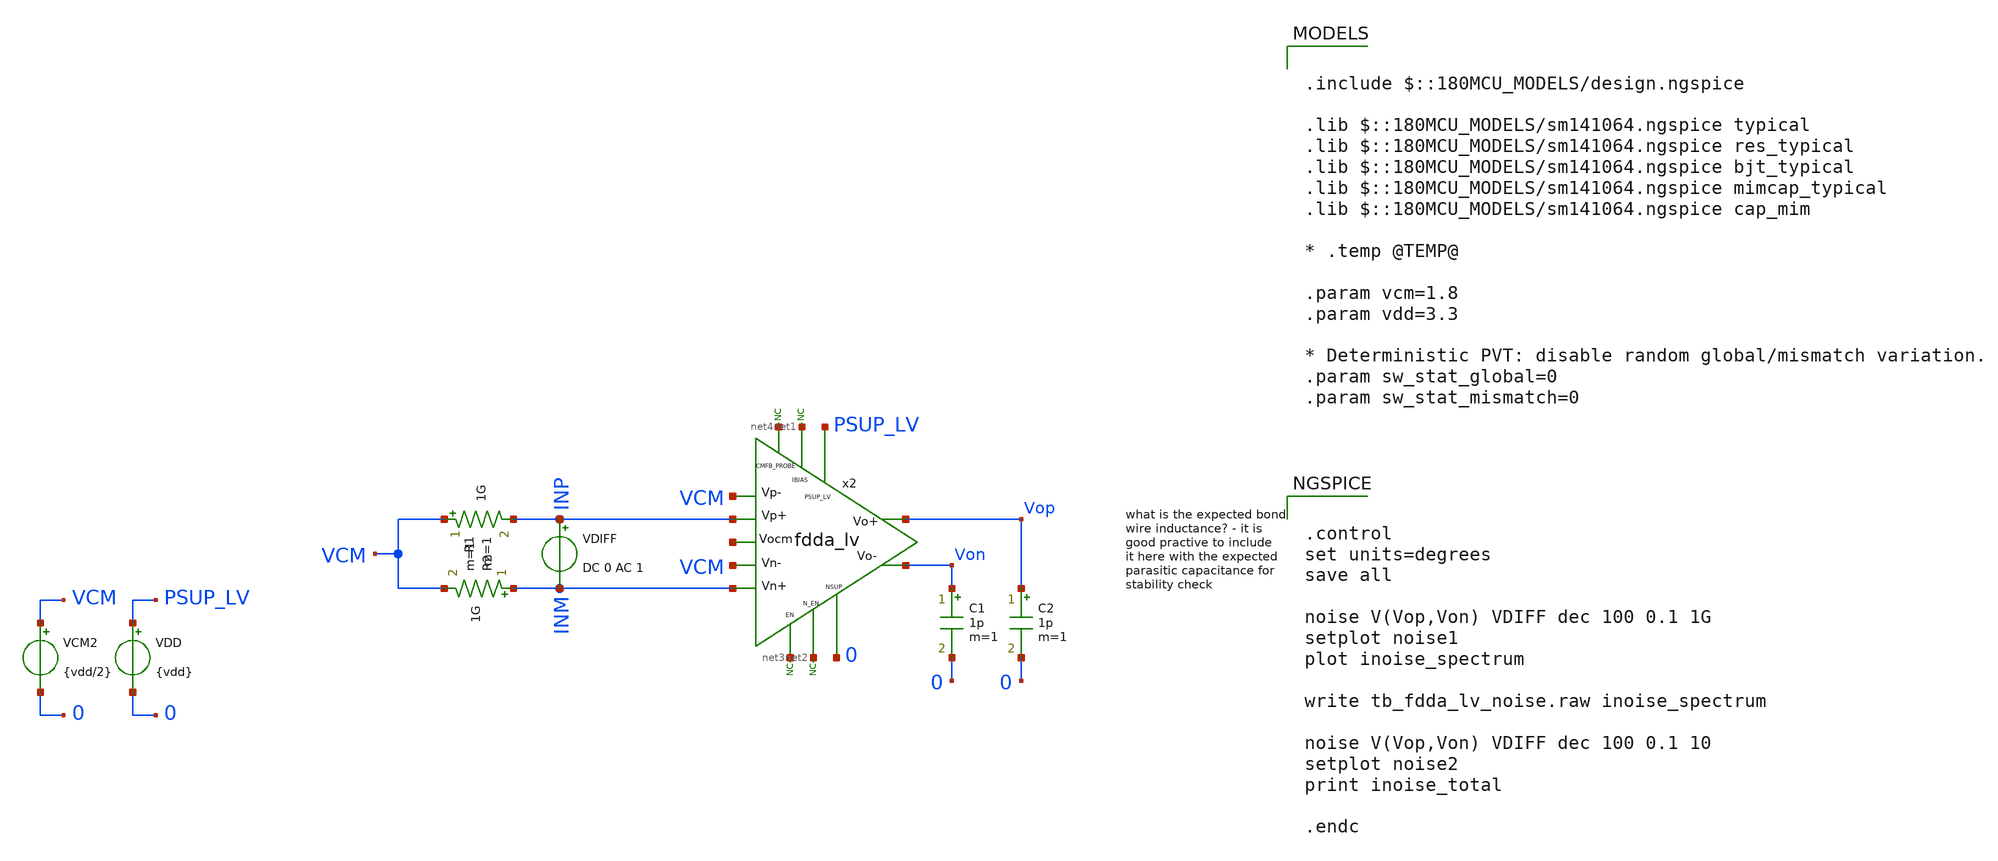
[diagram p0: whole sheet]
** sch_path: xschem/blocks/fdda_lv/tb_fdda_lv_noise.sch
**.subckt tb_fdda_lv_noise
C1 Von 0 1p m=1
x2 PSUP_LV VCM VCM INM INP Vop Von net1 net2 net3 0 net4 net5 fdda_lv
* noconn #net1
* noconn #net3
* noconn #net2
VDD PSUP_LV 0 {vdd}
C2 Vop 0 1p m=1
VCM2 VCM 0 {vdd/2}
* noconn #net4
VDIFF INP INM DC 0 AC 1
R1 VCM INP 1G m=1
R2 INM VCM 1G m=1
**** begin user architecture code

.include $::180MCU_MODELS/design.ngspice

.lib $::180MCU_MODELS/sm141064.ngspice typical
.lib $::180MCU_MODELS/sm141064.ngspice res_typical
.lib $::180MCU_MODELS/sm141064.ngspice bjt_typical
.lib $::180MCU_MODELS/sm141064.ngspice mimcap_typical
.lib $::180MCU_MODELS/sm141064.ngspice cap_mim

* .temp @TEMP@

.param vcm=1.8
.param vdd=3.3

* Deterministic PVT: disable random global/mismatch variation.
.param sw_stat_global=0
.param sw_stat_mismatch=0



.control
set units=degrees
save all

noise V(Vop,Von) VDIFF dec 100 0.1 1G
setplot noise1
plot inoise_spectrum

write tb_fdda_lv_noise.raw inoise_spectrum

noise V(Vop,Von) VDIFF dec 100 0.1 10
setplot noise2
print inoise_total

.endc


**** end user architecture code
**.ends
.end
